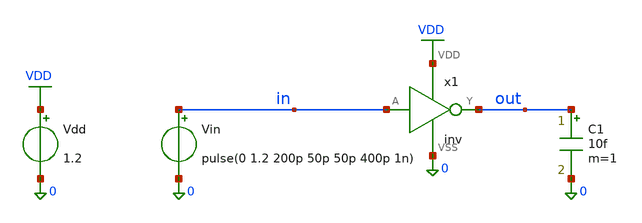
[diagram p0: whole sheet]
** sch_path: examples/ihp-inv/libs/cells/tb_inv/schematic/tb_inv.sch
**.subckt tb_inv
x1 in out VDD 0 inv
Vdd VDD 0 1.2
Vin in 0 pulse(0 1.2 200p 50p 50p 400p 1n)
C1 out 0 10f m=1
**.ends
.GLOBAL VDD
.end
